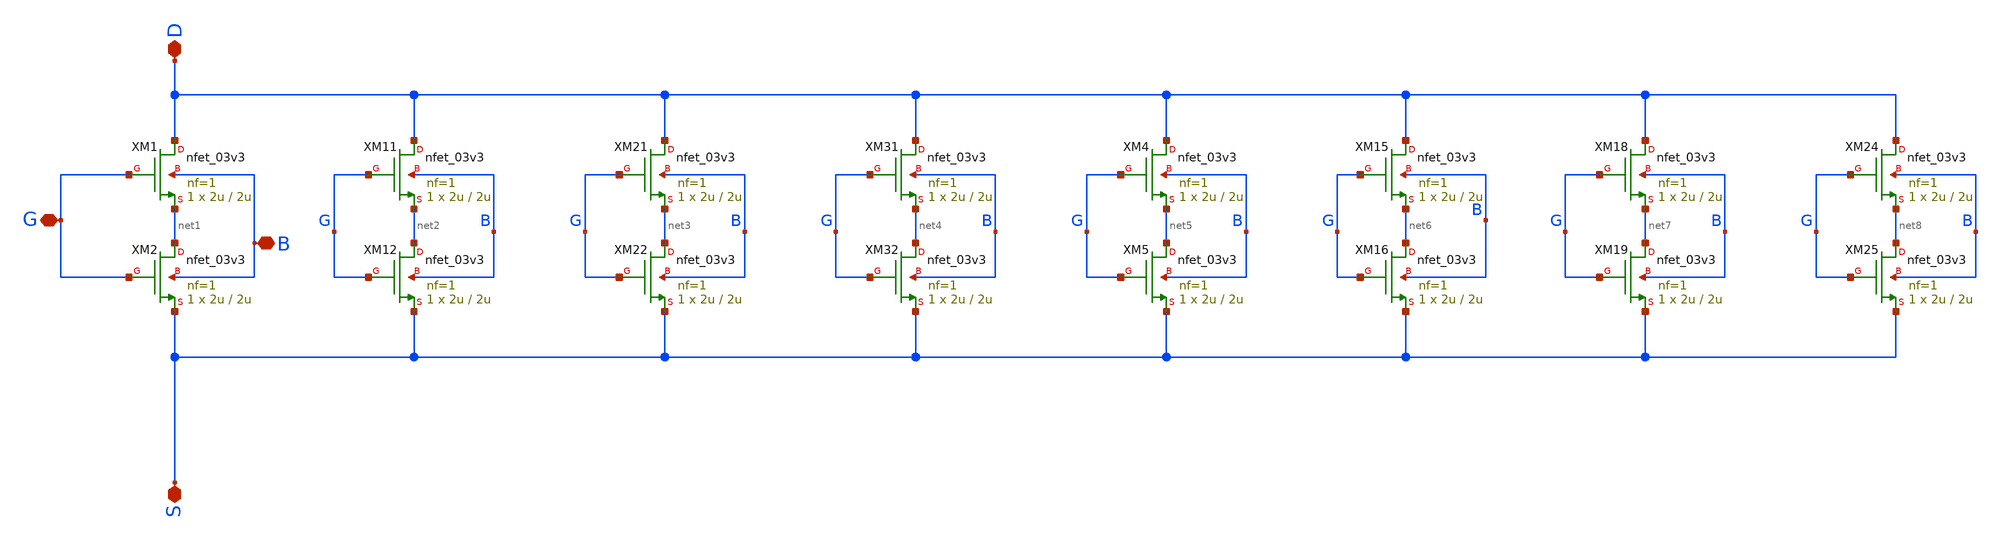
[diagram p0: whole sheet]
** sch_path: Voltage_Reference/symbols_vr/NMOS_matrix2_SCM2.sch
**.subckt NMOS_matrix2_SCM2 D G S B
*.iopin D
*.iopin G
*.iopin S
*.iopin B
XM1 D G net1 B nfet_03v3 L=2u W=2u nf=1 ad='int((nf+1)/2) * W/nf * 0.18u' as='int((nf+2)/2) * W/nf * 0.18u'
+ pd='2*int((nf+1)/2) * (W/nf + 0.18u)' ps='2*int((nf+2)/2) * (W/nf + 0.18u)' nrd='0.18u / W' nrs='0.18u / W'
+ sa=0 sb=0 sd=0 m=1
XM2 net1 G S B nfet_03v3 L=2u W=2u nf=1 ad='int((nf+1)/2) * W/nf * 0.18u' as='int((nf+2)/2) * W/nf * 0.18u'
+ pd='2*int((nf+1)/2) * (W/nf + 0.18u)' ps='2*int((nf+2)/2) * (W/nf + 0.18u)' nrd='0.18u / W' nrs='0.18u / W'
+ sa=0 sb=0 sd=0 m=1
XM11 D G net2 B nfet_03v3 L=2u W=2u nf=1 ad='int((nf+1)/2) * W/nf * 0.18u' as='int((nf+2)/2) * W/nf * 0.18u'
+ pd='2*int((nf+1)/2) * (W/nf + 0.18u)' ps='2*int((nf+2)/2) * (W/nf + 0.18u)' nrd='0.18u / W' nrs='0.18u / W'
+ sa=0 sb=0 sd=0 m=1
XM12 net2 G S B nfet_03v3 L=2u W=2u nf=1 ad='int((nf+1)/2) * W/nf * 0.18u' as='int((nf+2)/2) * W/nf * 0.18u'
+ pd='2*int((nf+1)/2) * (W/nf + 0.18u)' ps='2*int((nf+2)/2) * (W/nf + 0.18u)' nrd='0.18u / W' nrs='0.18u / W'
+ sa=0 sb=0 sd=0 m=1
XM21 D G net3 B nfet_03v3 L=2u W=2u nf=1 ad='int((nf+1)/2) * W/nf * 0.18u' as='int((nf+2)/2) * W/nf * 0.18u'
+ pd='2*int((nf+1)/2) * (W/nf + 0.18u)' ps='2*int((nf+2)/2) * (W/nf + 0.18u)' nrd='0.18u / W' nrs='0.18u / W'
+ sa=0 sb=0 sd=0 m=1
XM22 net3 G S B nfet_03v3 L=2u W=2u nf=1 ad='int((nf+1)/2) * W/nf * 0.18u' as='int((nf+2)/2) * W/nf * 0.18u'
+ pd='2*int((nf+1)/2) * (W/nf + 0.18u)' ps='2*int((nf+2)/2) * (W/nf + 0.18u)' nrd='0.18u / W' nrs='0.18u / W'
+ sa=0 sb=0 sd=0 m=1
XM31 D G net4 B nfet_03v3 L=2u W=2u nf=1 ad='int((nf+1)/2) * W/nf * 0.18u' as='int((nf+2)/2) * W/nf * 0.18u'
+ pd='2*int((nf+1)/2) * (W/nf + 0.18u)' ps='2*int((nf+2)/2) * (W/nf + 0.18u)' nrd='0.18u / W' nrs='0.18u / W'
+ sa=0 sb=0 sd=0 m=1
XM32 net4 G S B nfet_03v3 L=2u W=2u nf=1 ad='int((nf+1)/2) * W/nf * 0.18u' as='int((nf+2)/2) * W/nf * 0.18u'
+ pd='2*int((nf+1)/2) * (W/nf + 0.18u)' ps='2*int((nf+2)/2) * (W/nf + 0.18u)' nrd='0.18u / W' nrs='0.18u / W'
+ sa=0 sb=0 sd=0 m=1
XM4 D G net5 B nfet_03v3 L=2u W=2u nf=1 ad='int((nf+1)/2) * W/nf * 0.18u' as='int((nf+2)/2) * W/nf * 0.18u'
+ pd='2*int((nf+1)/2) * (W/nf + 0.18u)' ps='2*int((nf+2)/2) * (W/nf + 0.18u)' nrd='0.18u / W' nrs='0.18u / W'
+ sa=0 sb=0 sd=0 m=1
XM5 net5 G S B nfet_03v3 L=2u W=2u nf=1 ad='int((nf+1)/2) * W/nf * 0.18u' as='int((nf+2)/2) * W/nf * 0.18u'
+ pd='2*int((nf+1)/2) * (W/nf + 0.18u)' ps='2*int((nf+2)/2) * (W/nf + 0.18u)' nrd='0.18u / W' nrs='0.18u / W'
+ sa=0 sb=0 sd=0 m=1
XM15 D G net6 B nfet_03v3 L=2u W=2u nf=1 ad='int((nf+1)/2) * W/nf * 0.18u' as='int((nf+2)/2) * W/nf * 0.18u'
+ pd='2*int((nf+1)/2) * (W/nf + 0.18u)' ps='2*int((nf+2)/2) * (W/nf + 0.18u)' nrd='0.18u / W' nrs='0.18u / W'
+ sa=0 sb=0 sd=0 m=1
XM16 net6 G S B nfet_03v3 L=2u W=2u nf=1 ad='int((nf+1)/2) * W/nf * 0.18u' as='int((nf+2)/2) * W/nf * 0.18u'
+ pd='2*int((nf+1)/2) * (W/nf + 0.18u)' ps='2*int((nf+2)/2) * (W/nf + 0.18u)' nrd='0.18u / W' nrs='0.18u / W'
+ sa=0 sb=0 sd=0 m=1
XM18 D G net7 B nfet_03v3 L=2u W=2u nf=1 ad='int((nf+1)/2) * W/nf * 0.18u' as='int((nf+2)/2) * W/nf * 0.18u'
+ pd='2*int((nf+1)/2) * (W/nf + 0.18u)' ps='2*int((nf+2)/2) * (W/nf + 0.18u)' nrd='0.18u / W' nrs='0.18u / W'
+ sa=0 sb=0 sd=0 m=1
XM19 net7 G S B nfet_03v3 L=2u W=2u nf=1 ad='int((nf+1)/2) * W/nf * 0.18u' as='int((nf+2)/2) * W/nf * 0.18u'
+ pd='2*int((nf+1)/2) * (W/nf + 0.18u)' ps='2*int((nf+2)/2) * (W/nf + 0.18u)' nrd='0.18u / W' nrs='0.18u / W'
+ sa=0 sb=0 sd=0 m=1
XM24 D G net8 B nfet_03v3 L=2u W=2u nf=1 ad='int((nf+1)/2) * W/nf * 0.18u' as='int((nf+2)/2) * W/nf * 0.18u'
+ pd='2*int((nf+1)/2) * (W/nf + 0.18u)' ps='2*int((nf+2)/2) * (W/nf + 0.18u)' nrd='0.18u / W' nrs='0.18u / W'
+ sa=0 sb=0 sd=0 m=1
XM25 net8 G S B nfet_03v3 L=2u W=2u nf=1 ad='int((nf+1)/2) * W/nf * 0.18u' as='int((nf+2)/2) * W/nf * 0.18u'
+ pd='2*int((nf+1)/2) * (W/nf + 0.18u)' ps='2*int((nf+2)/2) * (W/nf + 0.18u)' nrd='0.18u / W' nrs='0.18u / W'
+ sa=0 sb=0 sd=0 m=1
**.ends
.end
